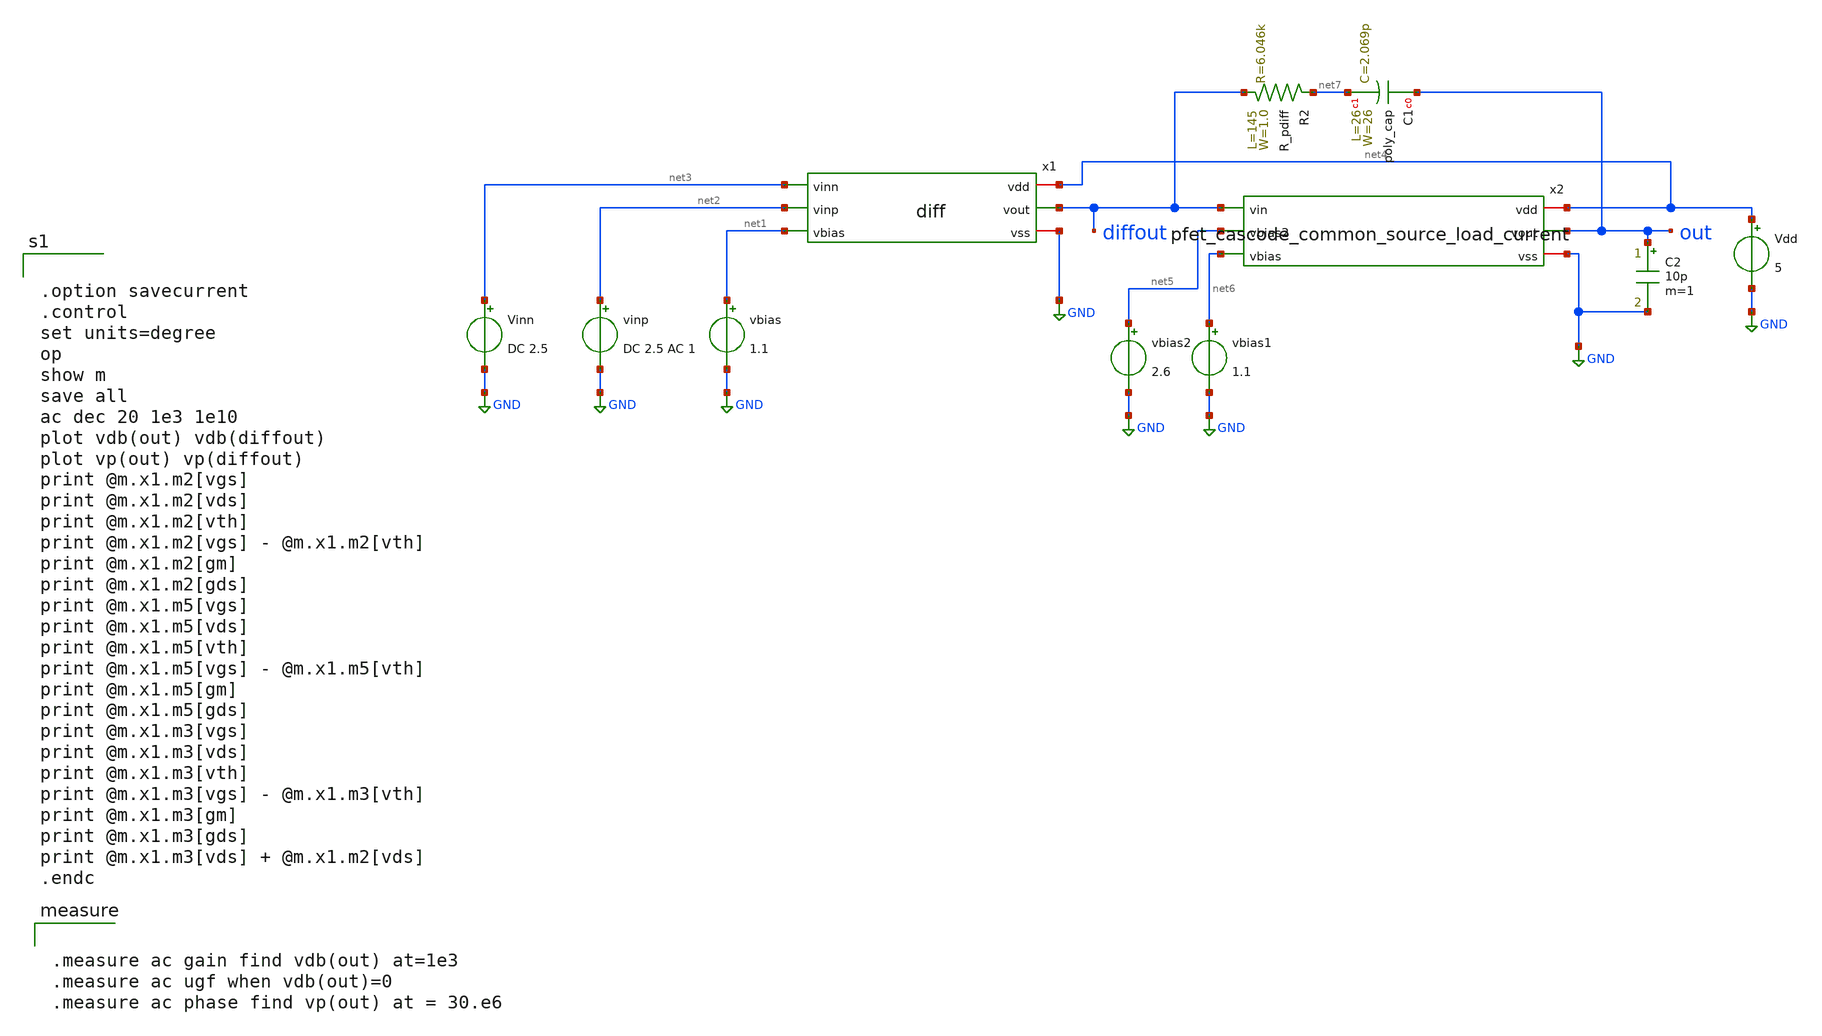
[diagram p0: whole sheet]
** sch_path: member_project/GroupWork/Team_masahiro/diff+cascode_source_common.sch
**.subckt diff+cascode_source_common
x1 net4 diffout net3 net2 net1 GND diff
Vinn net3 GND DC 2.5
vinp net2 GND DC 2.5 AC 1
vbias net1 GND 1.1
Vdd net4 GND 5
vbias1 net6 GND 1.1
x2 net4 diffout net5 out net6 GND pfet_cascode_common_source_load_current
vbias2 net5 GND 2.6
C2 out GND 10p m=1
C1 out net7 poly_cap W=26 L=26
R2 diffout net7 R_pdiff W=1.0 L=145
**** begin user architecture code
 .include $::LIB/mos.lib
.include $::LIB/passive.lib
.include $::LIB/diode.lib


.option savecurrent
.control
set units=degree
op
show m
save all
ac dec 20 1e3 1e10
plot vdb(out) vdb(diffout)
plot vp(out) vp(diffout)
print @m.x1.m2[vgs]
print @m.x1.m2[vds]
print @m.x1.m2[vth]
print @m.x1.m2[vgs] - @m.x1.m2[vth]
print @m.x1.m2[gm]
print @m.x1.m2[gds]
print @m.x1.m5[vgs]
print @m.x1.m5[vds]
print @m.x1.m5[vth]
print @m.x1.m5[vgs] - @m.x1.m5[vth]
print @m.x1.m5[gm]
print @m.x1.m5[gds]
print @m.x1.m3[vgs]
print @m.x1.m3[vds]
print @m.x1.m3[vth]
print @m.x1.m3[vgs] - @m.x1.m3[vth]
print @m.x1.m3[gm]
print @m.x1.m3[gds]
print @m.x1.m3[vds] + @m.x1.m2[vds]
.endc




.measure ac gain find vdb(out) at=1e3
.measure ac ugf when vdb(out)=0
.measure ac phase find vp(out) at = 30.e6


**** end user architecture code
**.ends

* expanding   symbol:  diff.sym # of pins=6
** sym_path: member_project/GroupWork/Team_masahiro/diff.sym
** sch_path: member_project/GroupWork/Team_masahiro/diff.sch
.subckt diff vdd vout vinn vinp vbias vss
*.iopin vss
*.iopin vdd
*.ipin vinn
*.ipin vinp
*.opin vout
*.ipin vbias
M1 net1 vinn net2 vss nmos L=2u W=100u m=1
M2 vout vinp net2 vss nmos L=2u W=100u m=1
M3 net2 vbias vss vss nmos L=2u W=20u m=1
M4 net1 net1 vdd vdd pmos L=2u W=35u m=1
M5 vout net1 vdd vdd pmos L=2u W=35u m=1
.ends


* expanding   symbol:  pfet_cascode_common_source_load_current.sym # of pins=6
** sym_path: member_project/GroupWork/Team_masahiro/pfet_cascode_common_source_load_current.sym
** sch_path: member_project/GroupWork/Team_masahiro/pfet_cascode_common_source_load_current.sch
.subckt pfet_cascode_common_source_load_current vdd vin vbias2 vout vbias vss
*.iopin vss
*.iopin vdd
*.ipin vin
*.opin vout
*.ipin vbias
*.ipin vbias2
M1 vout vbias vss vss nmos L=1u W=80u m=1
M2 net1 vin vdd vdd pmos L=1u W=160u m=1
M3 vout vbias2 net1 net1 pmos L=1u W=160u m=1
.ends

.GLOBAL GND
.end
